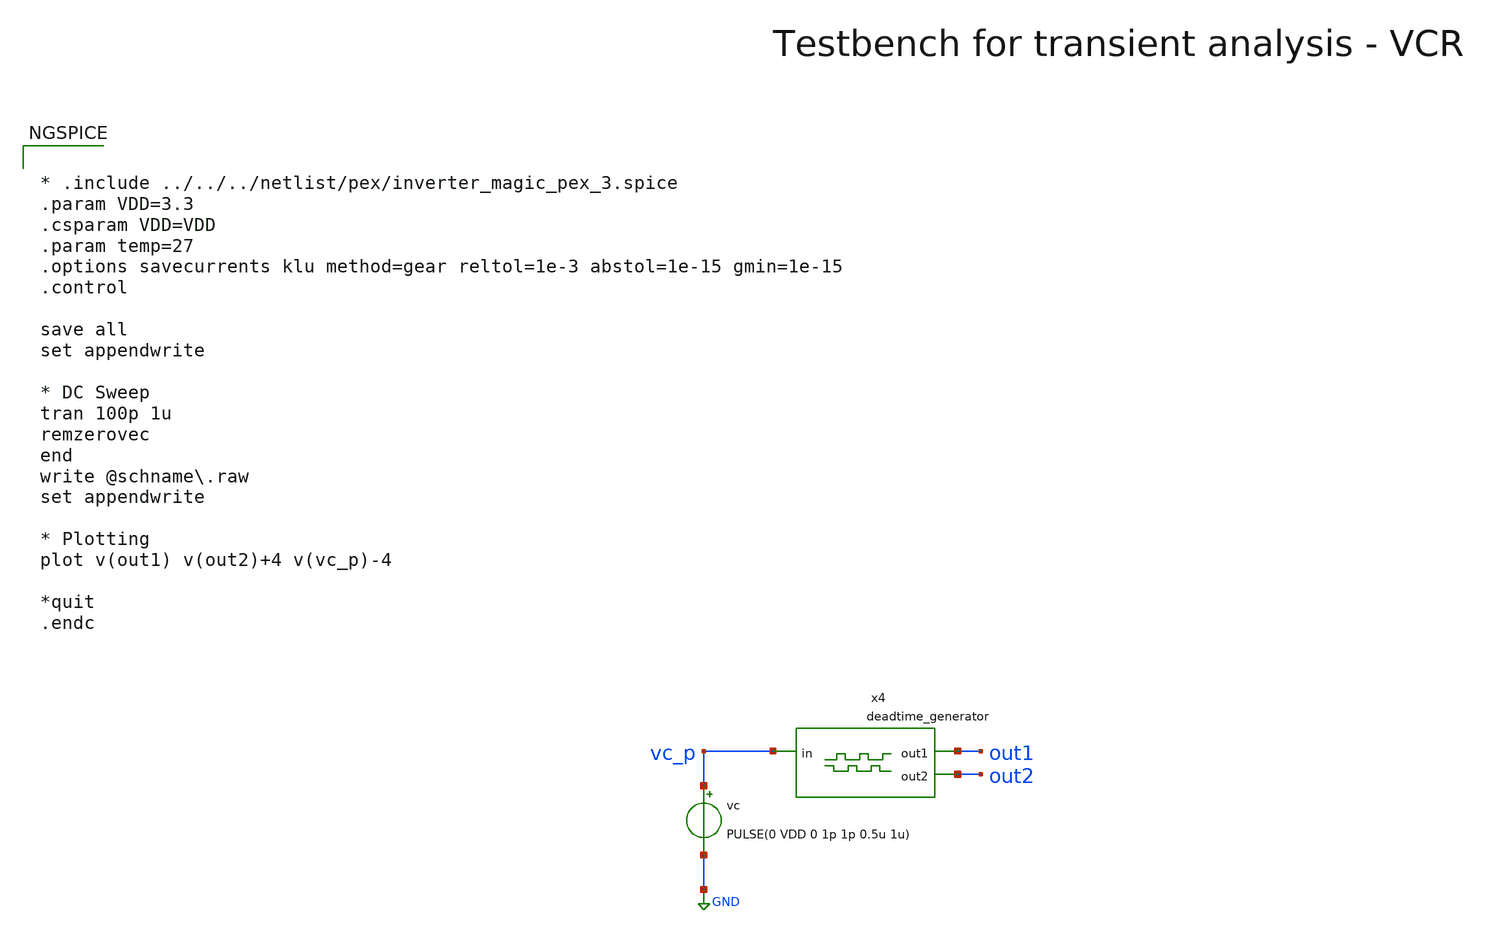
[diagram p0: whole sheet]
** sch_path: macros/heichips26_vcr/macros/switched_capacitor/testbenches/xschem/tb_tran_deadtime.sch
**.subckt tb_tran_deadtime
vc vc_p GND PULSE(0 VDD 0 1p 1p 0.5u 1u)
x4 vc_p out1 out2 deadtime_generator
**** begin user architecture code


* .include ../../../netlist/pex/inverter_magic_pex_3.spice
.param VDD=3.3
.csparam VDD=VDD
.param temp=27
.options savecurrents klu method=gear reltol=1e-3 abstol=1e-15 gmin=1e-15
.control

save all
set appendwrite

* DC Sweep
tran 100p 1u
remzerovec
end
write @schname\.raw
set appendwrite

* Plotting
plot v(out1) v(out2)+4 v(vc_p)-4

*quit
.endc



.lib cornerMOSlv.lib mos_tt
.lib cornerMOShv.lib mos_tt
.lib cornerRES.lib res_typ
.lib cornerDIO.lib dio_tt

.include $::PDK_ROOT/$::PDK/libs.ref/sg13cmos5l_stdcell/spice/sg13cmos5l_stdcell.spice

**** end user architecture code
**.ends

* expanding   symbol:  deadtime_generator.sym # of pins=3
** sym_path: macros/heichips26_vcr/macros/switched_capacitor/schematic/xschem/deadtime_generator.sym
** sch_path: macros/heichips26_vcr/macros/switched_capacitor/schematic/xschem/deadtime_generator.sch
.subckt deadtime_generator in out1 out2
*.ipin in
*.opin out1
*.opin out2
x4 net2 out1 net1 VDD VSS sg13cmos5l_nor2_1
x7 net1 in VDD VSS sg13cmos5l_inv_1
x5 net3 in out2 VDD VSS sg13cmos5l_nor2_1
x42 out1 net3 VDD VSS sg13cmos5l_dlygate4sd3_1
x1 out2 net2 VDD VSS sg13cmos5l_dlygate4sd3_1
.ends

.GLOBAL GND
.end
